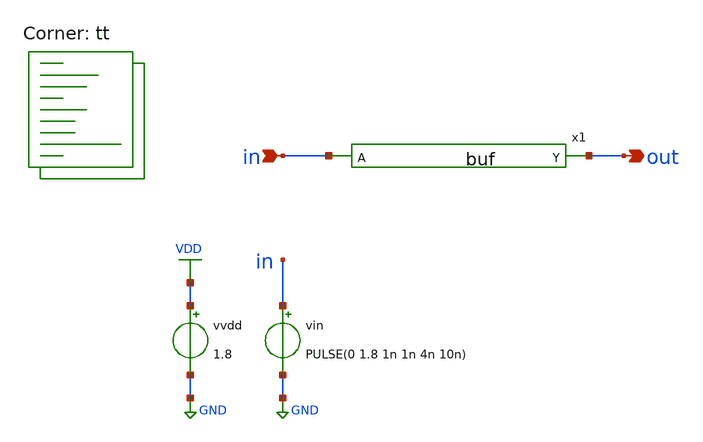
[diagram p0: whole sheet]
** sch_path: xschem/sim/tb_buf.sch
**.subckt tb_buf in out
*.ipin in
*.opin out
vvdd VDD GND 1.8
vin in GND PULSE(0 1.8 1n 1n 4n 10n)
x1 out in buf
**** begin user architecture code
.lib $::SKYWATER_MODELS/sky130.lib.spice tt


.control
* VTC analysis
DC vin 0 1.8 .1m
save all
let VP = 1.8
let vo_mid = VP/2
let dvout = deriv(v(out))
meas DC VSW find v(in) when v(out)=vo_mid
meas DC VOL MIN v(out) from=0 to=1.8
meas DC VOH MAX v(out) from=0 to=1.8
meas DC VIL find v(in) WHEN dvout=1 CROSS=1
meas DC VIH find v(in) WHEN dvout=1 CROSS=2

 VTC measurements
print VSW
print VIL
print VIH
print VOH
print VOL
echo
set filetype=binary
write tb_buf_vtc.raw v(out) v(in) dvout VSW VIL VIH VOH VOL

* Transient analysis
TRAN 0.01n 20n
save all
let VP=1.8
let per10 = VP*0.1
let per50 = VP*0.5
let per90 = VP*0.9
meas TRAN t_rise  TRIG v(out) VAL=per10 rise=1  TARG v(out) VAL=per90 rise=1
meas TRAN t_fall  TRIG v(out) VAL=per90 fall=1  TARG v(out) VAL=per10 fall=1
meas TRAN t_delay  TRIG v(in) VAL=per50 rise=1 TARG v(out) VAL=per50 fall=1
echo TRAN measurements
print t_delay
print t_rise
print t_fall
echo
set filetype=binary
write tb_buf_tran.raw
.endc


**** end user architecture code
**.ends

* expanding   symbol:  buf.sym # of pins=2
** sym_path: xschem/sim/buf.sym
** sch_path: xschem/sim/buf.sch
.subckt buf Y A
*.ipin A
*.opin Y
x1 A net1 inv
x2 net1 Y inv
.ends


* expanding   symbol:  inv.sym # of pins=2
** sym_path: xschem/sim/inv.sym
** sch_path: xschem/sim/inv.sch
.subckt inv A Y
*.opin Y
*.ipin A
XM1 Y A VDD VDD sky130_fd_pr__pfet_01v8 L=0.15 W=1.26 nf=1 ad='int((nf+1)/2) * W/nf * 0.29' as='int((nf+2)/2) * W/nf * 0.29'
+ pd='2*int((nf+1)/2) * (W/nf + 0.29)' ps='2*int((nf+2)/2) * (W/nf + 0.29)' nrd='0.29 / W' nrs='0.29 / W'
+ sa=0 sb=0 sd=0 mult=1 m=1
XM2 Y A GND GND sky130_fd_pr__nfet_01v8 L=0.15 W=0.52 nf=1 ad='int((nf+1)/2) * W/nf * 0.29' as='int((nf+2)/2) * W/nf * 0.29'
+ pd='2*int((nf+1)/2) * (W/nf + 0.29)' ps='2*int((nf+2)/2) * (W/nf + 0.29)' nrd='0.29 / W' nrs='0.29 / W'
+ sa=0 sb=0 sd=0 mult=1 m=1
.ends

.GLOBAL GND
.GLOBAL VDD
.end
